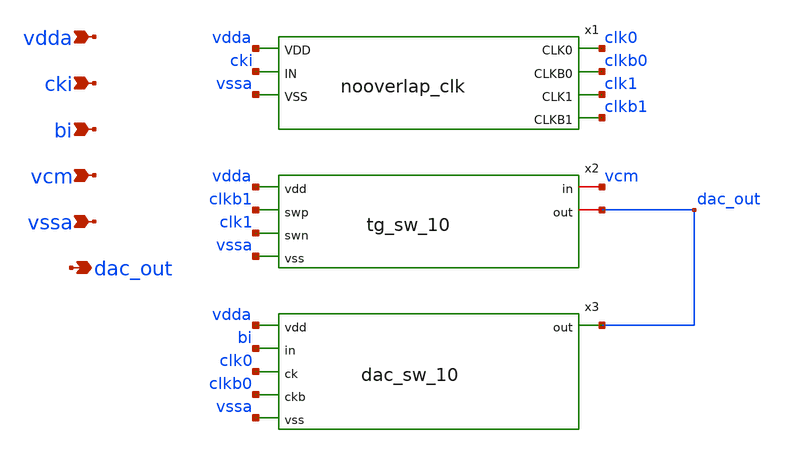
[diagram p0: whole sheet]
** sch_path: xschem/cdac_sw_10.sch
**.subckt cdac_sw_10 vdda cki bi vcm vssa dac_out
*.ipin vdda
*.ipin cki
*.ipin bi
*.ipin vcm
*.ipin vssa
*.opin dac_out
x1 vdda cki vssa clk0 clkb0 clk1 clkb1 nooverlap_clk
x2 vdda clkb1 clk1 vssa vcm dac_out tg_sw_10
x3 vdda bi clk0 clkb0 vssa dac_out dac_sw_10
**.ends

* expanding   symbol:  nooverlap_clk.sym # of pins=7
** sym_path: xschem/nooverlap_clk.sym
** sch_path: xschem/nooverlap_clk.sch
.subckt nooverlap_clk VDD IN VSS CLK0 CLKB0 CLK1 CLKB1
*.ipin VDD
*.ipin IN
*.ipin VSS
*.opin CLK0
*.opin CLKB0
*.opin CLK1
*.opin CLKB1
x1 IN a vss vss vdd vdd net5 sky130_fd_sc_hs__nand2_1
x2 b net1 vss vss vdd vdd net2 sky130_fd_sc_hs__nand2_1
x3 IN vss vss vdd vdd net1 sky130_fd_sc_hs__inv_1
x4 net5 vss vss vdd vdd net4 sky130_fd_sc_hs__inv_1
x5 net2 vss vss vdd vdd net3 sky130_fd_sc_hs__inv_1
x6 net4 vss vss vdd vdd b sky130_fd_sc_hs__inv_1
x7 net3 vss vss vdd vdd a sky130_fd_sc_hs__inv_1
x8 b vss vss vdd vdd net6 sky130_fd_sc_hs__inv_4
x9 a vss vss vdd vdd net7 sky130_fd_sc_hs__inv_4
x10 net6 vss vss vdd vdd CLKB0 sky130_fd_sc_hs__inv_8
x11 net7 vss vss vdd vdd CLKB1 sky130_fd_sc_hs__inv_8
x12 CLKB0 vss vss vdd vdd CLK0 sky130_fd_sc_hs__inv_8
x13 CLKB1 vss vss vdd vdd CLK1 sky130_fd_sc_hs__inv_8
**** begin user architecture code

.include /usr/local/share/pdk/sky130A/libs.ref/sky130_fd_sc_hs/spice/sky130_fd_sc_hs.spice

**** end user architecture code
.ends


* expanding   symbol:  tg_sw_10.sym # of pins=6
** sym_path: xschem/tg_sw_10.sym
** sch_path: xschem/tg_sw_10.sch
.subckt tg_sw_10 vdd swp swn vss in out
*.ipin vdd
*.ipin swp
*.ipin swn
*.ipin vss
*.iopin in
*.iopin out
XM1 in swp out vdd sky130_fd_pr__pfet_01v8 L=0.5 W=1.5 nf=1 ad='int((nf+1)/2) * W/nf * 0.29' as='int((nf+2)/2) * W/nf * 0.29'
+ pd='2*int((nf+1)/2) * (W/nf + 0.29)' ps='2*int((nf+2)/2) * (W/nf + 0.29)' nrd='0.29 / W' nrs='0.29 / W'
+ sa=0 sb=0 sd=0 mult=2 m=2
XM2 in swn out vss sky130_fd_pr__nfet_01v8 L=0.5 W=0.5 nf=1 ad='int((nf+1)/2) * W/nf * 0.29' as='int((nf+2)/2) * W/nf * 0.29'
+ pd='2*int((nf+1)/2) * (W/nf + 0.29)' ps='2*int((nf+2)/2) * (W/nf + 0.29)' nrd='0.29 / W' nrs='0.29 / W'
+ sa=0 sb=0 sd=0 mult=2 m=2
.ends


* expanding   symbol:  dac_sw_10.sym # of pins=6
** sym_path: xschem/dac_sw_10.sym
** sch_path: xschem/dac_sw_10.sch
.subckt dac_sw_10 vdd in ck ckb vss out
*.ipin vdd
*.ipin in
*.ipin ck
*.ipin ckb
*.ipin vss
*.opin out
XM1 net1 in vdd vdd sky130_fd_pr__pfet_01v8 L=0.5 W=1.5 nf=1 ad='int((nf+1)/2) * W/nf * 0.29' as='int((nf+2)/2) * W/nf * 0.29'
+ pd='2*int((nf+1)/2) * (W/nf + 0.29)' ps='2*int((nf+2)/2) * (W/nf + 0.29)' nrd='0.29 / W' nrs='0.29 / W'
+ sa=0 sb=0 sd=0 mult=2 m=2
XM2 out ckb net1 vdd sky130_fd_pr__pfet_01v8 L=0.5 W=1.5 nf=1 ad='int((nf+1)/2) * W/nf * 0.29' as='int((nf+2)/2) * W/nf * 0.29'
+ pd='2*int((nf+1)/2) * (W/nf + 0.29)' ps='2*int((nf+2)/2) * (W/nf + 0.29)' nrd='0.29 / W' nrs='0.29 / W'
+ sa=0 sb=0 sd=0 mult=2 m=2
XM3 out ck net2 vss sky130_fd_pr__nfet_01v8 L=0.5 W=0.5 nf=1 ad='int((nf+1)/2) * W/nf * 0.29' as='int((nf+2)/2) * W/nf * 0.29'
+ pd='2*int((nf+1)/2) * (W/nf + 0.29)' ps='2*int((nf+2)/2) * (W/nf + 0.29)' nrd='0.29 / W' nrs='0.29 / W'
+ sa=0 sb=0 sd=0 mult=2 m=2
XM4 net2 in vss vss sky130_fd_pr__nfet_01v8 L=0.5 W=0.5 nf=1 ad='int((nf+1)/2) * W/nf * 0.29' as='int((nf+2)/2) * W/nf * 0.29'
+ pd='2*int((nf+1)/2) * (W/nf + 0.29)' ps='2*int((nf+2)/2) * (W/nf + 0.29)' nrd='0.29 / W' nrs='0.29 / W'
+ sa=0 sb=0 sd=0 mult=2 m=2
.ends

.end
